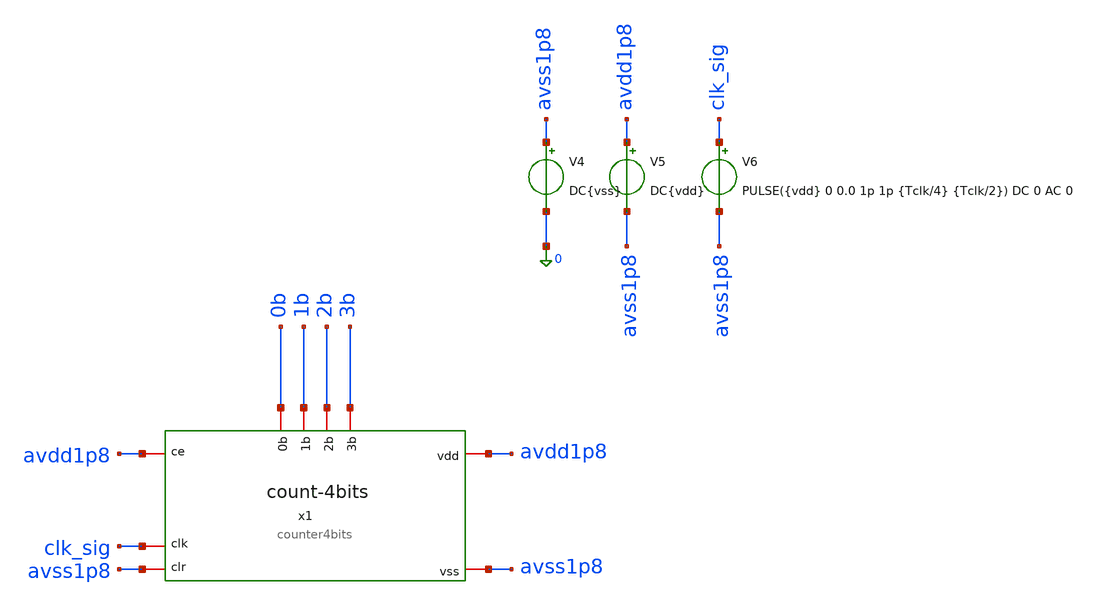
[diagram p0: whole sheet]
** sch_path: design/tb_counter4bits.sch
**.subckt tb_counter4bits
x1 avss1p8 avdd1p8 0b avdd1p8 avss1p8 clk_sig 1b 2b 3b counter4bits
V4 avss1p8 0 DC{vss}
V5 avdd1p8 avss1p8 DC{vdd}
V6 clk_sig avss1p8 PULSE({vdd} 0 0.0 1p 1p {Tclk/4} {Tclk/2}) DC 0 AC 0
**** begin user architecture code


* Circuit Parameters
.param vdd = 1.2
.param vss = 0.0
.param Tclk = 10n
.options TEMP = 27.0
* Include Models - IHP SG13G2
.lib cornerMOSlv.lib mos_tt
* OP Parameters & Singals to save
.save all
*Simulations
.control
tran 0.01u 100n
setplot tran1
plot v(clk_sig) v(0b)+1.2 v(1b)+2.4 v(2b)+3.6 v(3b)+4.8
reset
dc V6 0 1.2 0.01
setplot dc
set filetype = ascii
write dcsweep.raw
.endc
.end


**** end user architecture code
**.ends
.end
